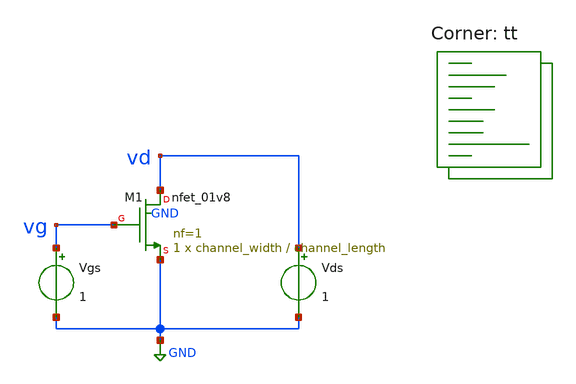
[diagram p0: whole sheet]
** sch_path: xschem/nfet1v8_params_tb.sch
**.subckt nfet1v8_params_tb
Vgs vg GND 1
Vds vd GND 1
XM1 vd vg GND GND sky130_fd_pr__nfet_01v8 L=channel_length W=channel_width nf=1 ad='int((nf+1)/2) * W/nf * 0.29'
+ as='int((nf+2)/2) * W/nf * 0.29' pd='2*int((nf+1)/2) * (W/nf + 0.29)' ps='2*int((nf+2)/2) * (W/nf + 0.29)'
+ nrd='0.29 / W' nrs='0.29 / W' sa=0 sb=0 sd=0 mult=1 m=1
**** begin user architecture code
.lib $::SKYWATER_MODELS/sky130.lib.spice tt


*.control
*dc vds 0.1 1.8 0.1 vgs 0.4 1.8 0.2
*plot -I(vds)
*dc vgs 0.4 1.8 0.1 vds 0.1 1.7 0.5
*plot -I(vds)
*save all
*write tb_gain.raw
*.endc




.param channel_width=3
.param channel_length=0.15


**** end user architecture code
**.ends
.GLOBAL GND
.end
